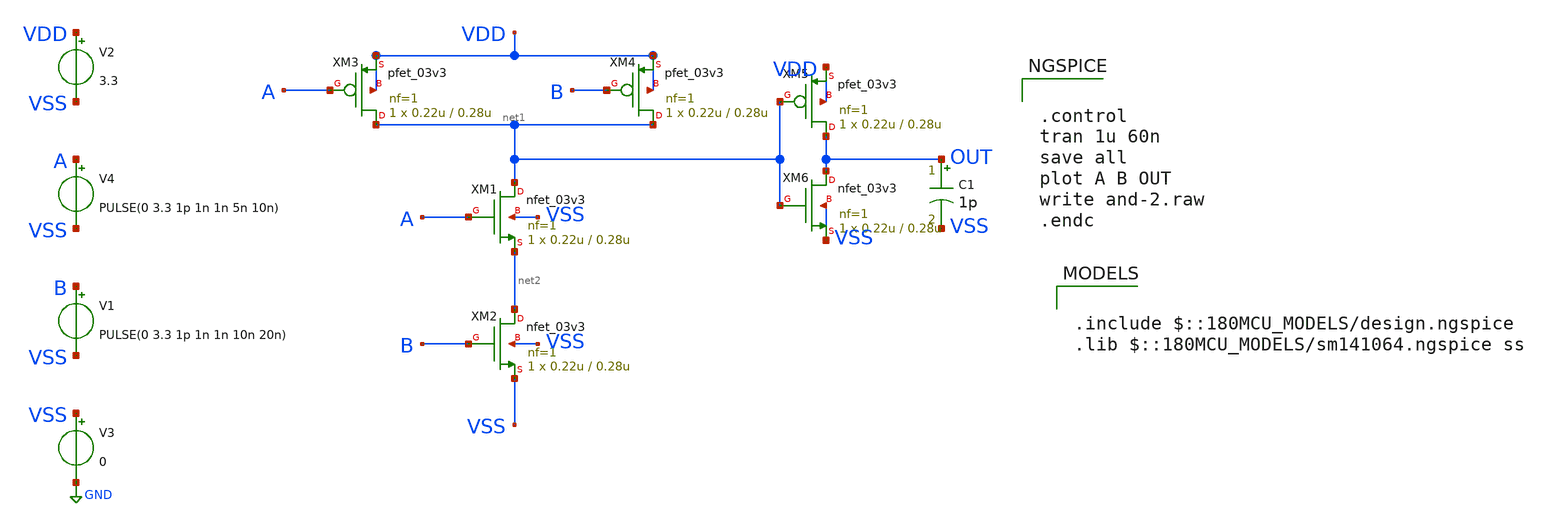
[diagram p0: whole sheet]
** sch_path: week02_current_diffpair/tugas5_cascode_current_mirror/and-2.sch
**.subckt and-2
XM1 net1 A net2 VSS nfet_03v3 L=0.28u W=0.22u nf=1 ad='int((nf+1)/2) * W/nf * 0.18u' as='int((nf+2)/2) * W/nf * 0.18u'
+ pd='2*int((nf+1)/2) * (W/nf + 0.18u)' ps='2*int((nf+2)/2) * (W/nf + 0.18u)' nrd='0.18u / W' nrs='0.18u / W'
+ sa=0 sb=0 sd=0 m=1
XM2 net2 B VSS VSS nfet_03v3 L=0.28u W=0.22u nf=1 ad='int((nf+1)/2) * W/nf * 0.18u' as='int((nf+2)/2) * W/nf * 0.18u'
+ pd='2*int((nf+1)/2) * (W/nf + 0.18u)' ps='2*int((nf+2)/2) * (W/nf + 0.18u)' nrd='0.18u / W' nrs='0.18u / W'
+ sa=0 sb=0 sd=0 m=1
XM3 net1 A VDD VDD pfet_03v3 L=0.28u W=0.22u nf=1 ad='int((nf+1)/2) * W/nf * 0.18u' as='int((nf+2)/2) * W/nf * 0.18u'
+ pd='2*int((nf+1)/2) * (W/nf + 0.18u)' ps='2*int((nf+2)/2) * (W/nf + 0.18u)' nrd='0.18u / W' nrs='0.18u / W'
+ sa=0 sb=0 sd=0 m=1
XM4 net1 B VDD VDD pfet_03v3 L=0.28u W=0.22u nf=1 ad='int((nf+1)/2) * W/nf * 0.18u' as='int((nf+2)/2) * W/nf * 0.18u'
+ pd='2*int((nf+1)/2) * (W/nf + 0.18u)' ps='2*int((nf+2)/2) * (W/nf + 0.18u)' nrd='0.18u / W' nrs='0.18u / W'
+ sa=0 sb=0 sd=0 m=1
V1 B VSS PULSE(0 3.3 1p 1n 1n 10n 20n)
V2 VDD VSS 3.3
V3 VSS GND 0
V4 A VSS PULSE(0 3.3 1p 1n 1n 5n 10n)
XM5 OUT net1 VDD VDD pfet_03v3 L=0.28u W=0.22u nf=1 ad='int((nf+1)/2) * W/nf * 0.18u' as='int((nf+2)/2) * W/nf * 0.18u'
+ pd='2*int((nf+1)/2) * (W/nf + 0.18u)' ps='2*int((nf+2)/2) * (W/nf + 0.18u)' nrd='0.18u / W' nrs='0.18u / W'
+ sa=0 sb=0 sd=0 m=1
XM6 OUT net1 VSS VSS nfet_03v3 L=0.28u W=0.22u nf=1 ad='int((nf+1)/2) * W/nf * 0.18u' as='int((nf+2)/2) * W/nf * 0.18u'
+ pd='2*int((nf+1)/2) * (W/nf + 0.18u)' ps='2*int((nf+2)/2) * (W/nf + 0.18u)' nrd='0.18u / W' nrs='0.18u / W'
+ sa=0 sb=0 sd=0 m=1
C1 OUT VSS 1p m=1
**** begin user architecture code

.include $::180MCU_MODELS/design.ngspice
.lib $::180MCU_MODELS/sm141064.ngspice ss



.control
tran 1u 60n
save all
plot A B OUT
write and-2.raw
.endc


**** end user architecture code
**.ends
.GLOBAL GND
.end
